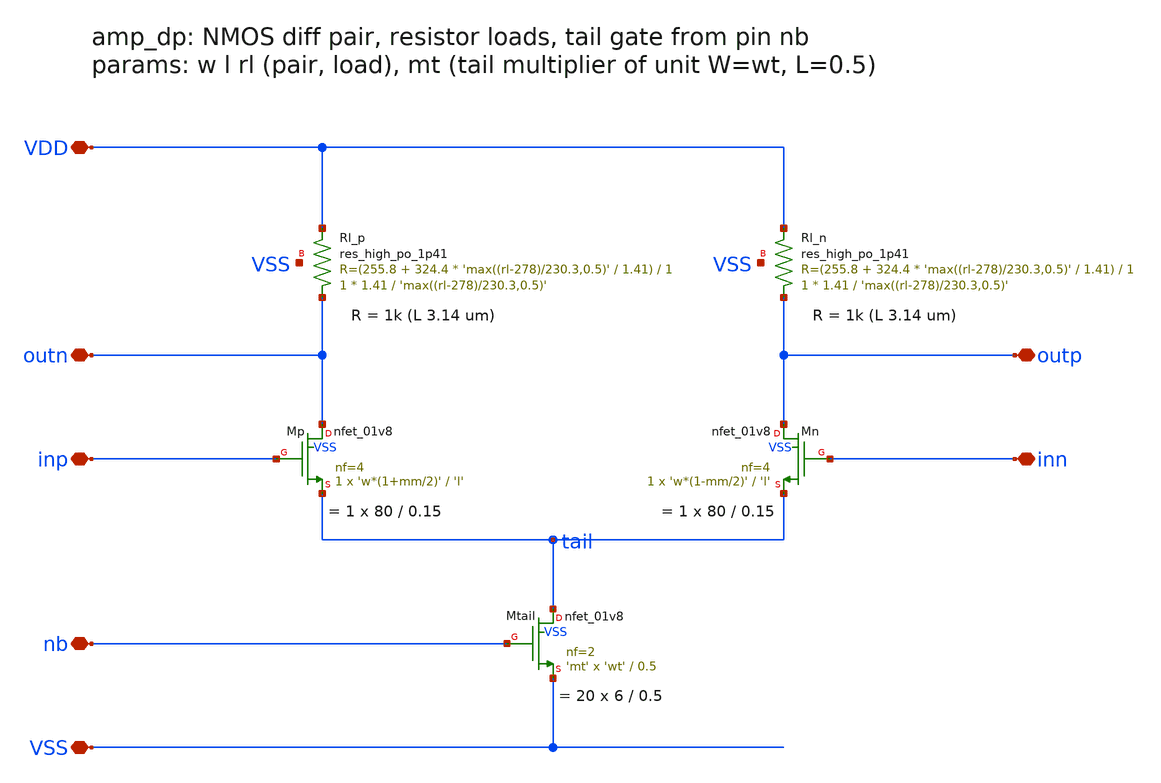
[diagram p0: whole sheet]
** sch_path: xschem/amp_dp.sch
**.subckt amp_dp VDD VSS nb inp inn outp outn
*.iopin VDD
*.iopin VSS
*.iopin nb
*.iopin inp
*.iopin inn
*.iopin outp
*.iopin outn
XRl_p outn VDD VSS sky130_fd_pr__res_high_po_1p41 L='max((rl-278)/230.3,0.5)' mult=1 m=1
XMp outn inp tail VSS sky130_fd_pr__nfet_01v8 L='l' W='w*(1+mm/2)' nf=4 ad='int((nf+1)/2) * W/nf * 0.29'
+ as='int((nf+2)/2) * W/nf * 0.29' pd='2*int((nf+1)/2) * (W/nf + 0.29)' ps='2*int((nf+2)/2) * (W/nf + 0.29)'
+ nrd='0.29 / W' nrs='0.29 / W' sa=0 sb=0 sd=0 mult=1 m=1
XRl_n outp VDD VSS sky130_fd_pr__res_high_po_1p41 L='max((rl-278)/230.3,0.5)' mult=1 m=1
XMn outp inn tail VSS sky130_fd_pr__nfet_01v8 L='l' W='w*(1-mm/2)' nf=4 ad='int((nf+1)/2) * W/nf * 0.29'
+ as='int((nf+2)/2) * W/nf * 0.29' pd='2*int((nf+1)/2) * (W/nf + 0.29)' ps='2*int((nf+2)/2) * (W/nf + 0.29)'
+ nrd='0.29 / W' nrs='0.29 / W' sa=0 sb=0 sd=0 mult=1 m=1
XMtail tail nb VSS VSS sky130_fd_pr__nfet_01v8 L=0.5 W='wt' nf=2 ad='int((nf+1)/2) * W/nf * 0.29' as='int((nf+2)/2) * W/nf * 0.29'
+ pd='2*int((nf+1)/2) * (W/nf + 0.29)' ps='2*int((nf+2)/2) * (W/nf + 0.29)' nrd='0.29 / W' nrs='0.29 / W'
+ sa=0 sb=0 sd=0 mult='mt' m='mt'
**.ends
.end
